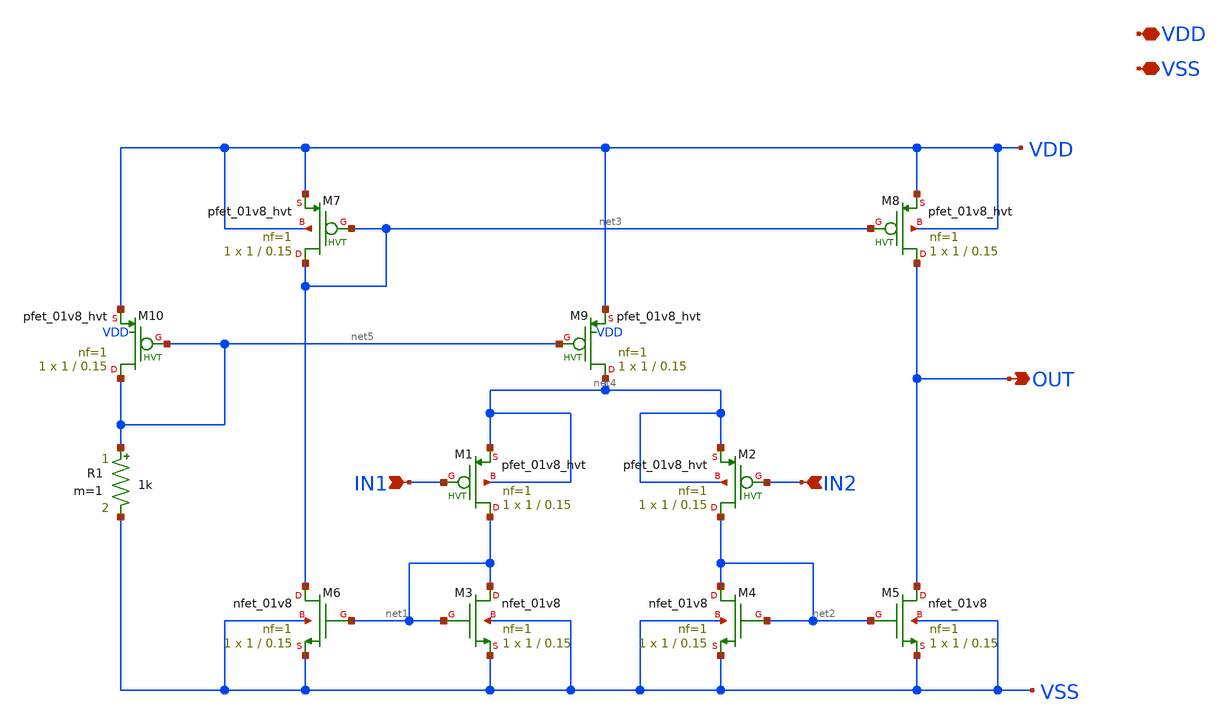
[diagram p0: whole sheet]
** sch_path: xschem/OTA_Simmetrico.sch
**.subckt OTA_Simmetrico VDD VSS IN1 IN2 OUT
*.iopin VDD
*.iopin VSS
*.ipin IN1
*.ipin IN2
*.opin OUT
XM1 net1 IN1 net4 net4 sky130_fd_pr__pfet_01v8_hvt L=0.15 W=1 nf=1 ad='int((nf+1)/2) * W/nf * 0.29' as='int((nf+2)/2) * W/nf * 0.29'
+ pd='2*int((nf+1)/2) * (W/nf + 0.29)' ps='2*int((nf+2)/2) * (W/nf + 0.29)' nrd='0.29 / W' nrs='0.29 / W'
+ sa=0 sb=0 sd=0 mult=1 m=1
XM2 net2 IN2 net4 net4 sky130_fd_pr__pfet_01v8_hvt L=0.15 W=1 nf=1 ad='int((nf+1)/2) * W/nf * 0.29' as='int((nf+2)/2) * W/nf * 0.29'
+ pd='2*int((nf+1)/2) * (W/nf + 0.29)' ps='2*int((nf+2)/2) * (W/nf + 0.29)' nrd='0.29 / W' nrs='0.29 / W'
+ sa=0 sb=0 sd=0 mult=1 m=1
XM3 net1 net1 VSS VSS sky130_fd_pr__nfet_01v8 L=0.15 W=1 nf=1 ad='int((nf+1)/2) * W/nf * 0.29' as='int((nf+2)/2) * W/nf * 0.29'
+ pd='2*int((nf+1)/2) * (W/nf + 0.29)' ps='2*int((nf+2)/2) * (W/nf + 0.29)' nrd='0.29 / W' nrs='0.29 / W'
+ sa=0 sb=0 sd=0 mult=1 m=1
XM4 net2 net2 VSS VSS sky130_fd_pr__nfet_01v8 L=0.15 W=1 nf=1 ad='int((nf+1)/2) * W/nf * 0.29' as='int((nf+2)/2) * W/nf * 0.29'
+ pd='2*int((nf+1)/2) * (W/nf + 0.29)' ps='2*int((nf+2)/2) * (W/nf + 0.29)' nrd='0.29 / W' nrs='0.29 / W'
+ sa=0 sb=0 sd=0 mult=1 m=1
XM5 OUT net2 VSS VSS sky130_fd_pr__nfet_01v8 L=0.15 W=1 nf=1 ad='int((nf+1)/2) * W/nf * 0.29' as='int((nf+2)/2) * W/nf * 0.29'
+ pd='2*int((nf+1)/2) * (W/nf + 0.29)' ps='2*int((nf+2)/2) * (W/nf + 0.29)' nrd='0.29 / W' nrs='0.29 / W'
+ sa=0 sb=0 sd=0 mult=1 m=1
XM6 net3 net1 VSS VSS sky130_fd_pr__nfet_01v8 L=0.15 W=1 nf=1 ad='int((nf+1)/2) * W/nf * 0.29' as='int((nf+2)/2) * W/nf * 0.29'
+ pd='2*int((nf+1)/2) * (W/nf + 0.29)' ps='2*int((nf+2)/2) * (W/nf + 0.29)' nrd='0.29 / W' nrs='0.29 / W'
+ sa=0 sb=0 sd=0 mult=1 m=1
XM7 net3 net3 VDD VDD sky130_fd_pr__pfet_01v8_hvt L=0.15 W=1 nf=1 ad='int((nf+1)/2) * W/nf * 0.29' as='int((nf+2)/2) * W/nf * 0.29'
+ pd='2*int((nf+1)/2) * (W/nf + 0.29)' ps='2*int((nf+2)/2) * (W/nf + 0.29)' nrd='0.29 / W' nrs='0.29 / W'
+ sa=0 sb=0 sd=0 mult=1 m=1
XM8 OUT net3 VDD VDD sky130_fd_pr__pfet_01v8_hvt L=0.15 W=1 nf=1 ad='int((nf+1)/2) * W/nf * 0.29' as='int((nf+2)/2) * W/nf * 0.29'
+ pd='2*int((nf+1)/2) * (W/nf + 0.29)' ps='2*int((nf+2)/2) * (W/nf + 0.29)' nrd='0.29 / W' nrs='0.29 / W'
+ sa=0 sb=0 sd=0 mult=1 m=1
XM9 net4 net5 VDD VDD sky130_fd_pr__pfet_01v8_hvt L=0.15 W=1 nf=1 ad='int((nf+1)/2) * W/nf * 0.29' as='int((nf+2)/2) * W/nf * 0.29'
+ pd='2*int((nf+1)/2) * (W/nf + 0.29)' ps='2*int((nf+2)/2) * (W/nf + 0.29)' nrd='0.29 / W' nrs='0.29 / W'
+ sa=0 sb=0 sd=0 mult=1 m=1
XM10 net5 net5 VDD VDD sky130_fd_pr__pfet_01v8_hvt L=0.15 W=1 nf=1 ad='int((nf+1)/2) * W/nf * 0.29' as='int((nf+2)/2) * W/nf * 0.29'
+ pd='2*int((nf+1)/2) * (W/nf + 0.29)' ps='2*int((nf+2)/2) * (W/nf + 0.29)' nrd='0.29 / W' nrs='0.29 / W'
+ sa=0 sb=0 sd=0 mult=1 m=1
R1 net5 VSS 1k m=1
**.ends
.end
